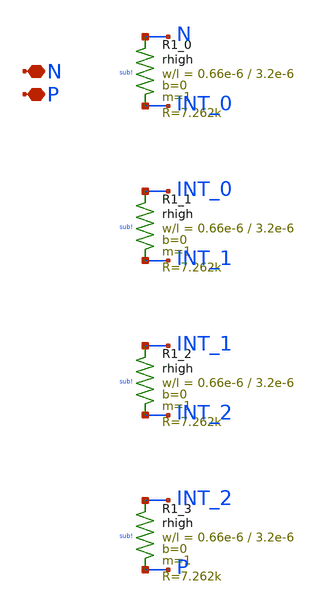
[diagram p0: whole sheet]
** sch_path: design/LELO_TR_IHP13G2/LELOTR_RES4.sch
**.subckt LELOTR_RES4 N P
*.iopin N
*.iopin P
XR1_0 N INT_0 sub! rhigh w=0.66e-6 l=3.2e-6 m=1 b=0 mm_ok=1
XR1_1 INT_0 INT_1 sub! rhigh w=0.66e-6 l=3.2e-6 m=1 b=0 mm_ok=1
XR1_2 INT_1 INT_2 sub! rhigh w=0.66e-6 l=3.2e-6 m=1 b=0 mm_ok=1
XR1_3 INT_2 P sub! rhigh w=0.66e-6 l=3.2e-6 m=1 b=0 mm_ok=1
**.ends
.end
